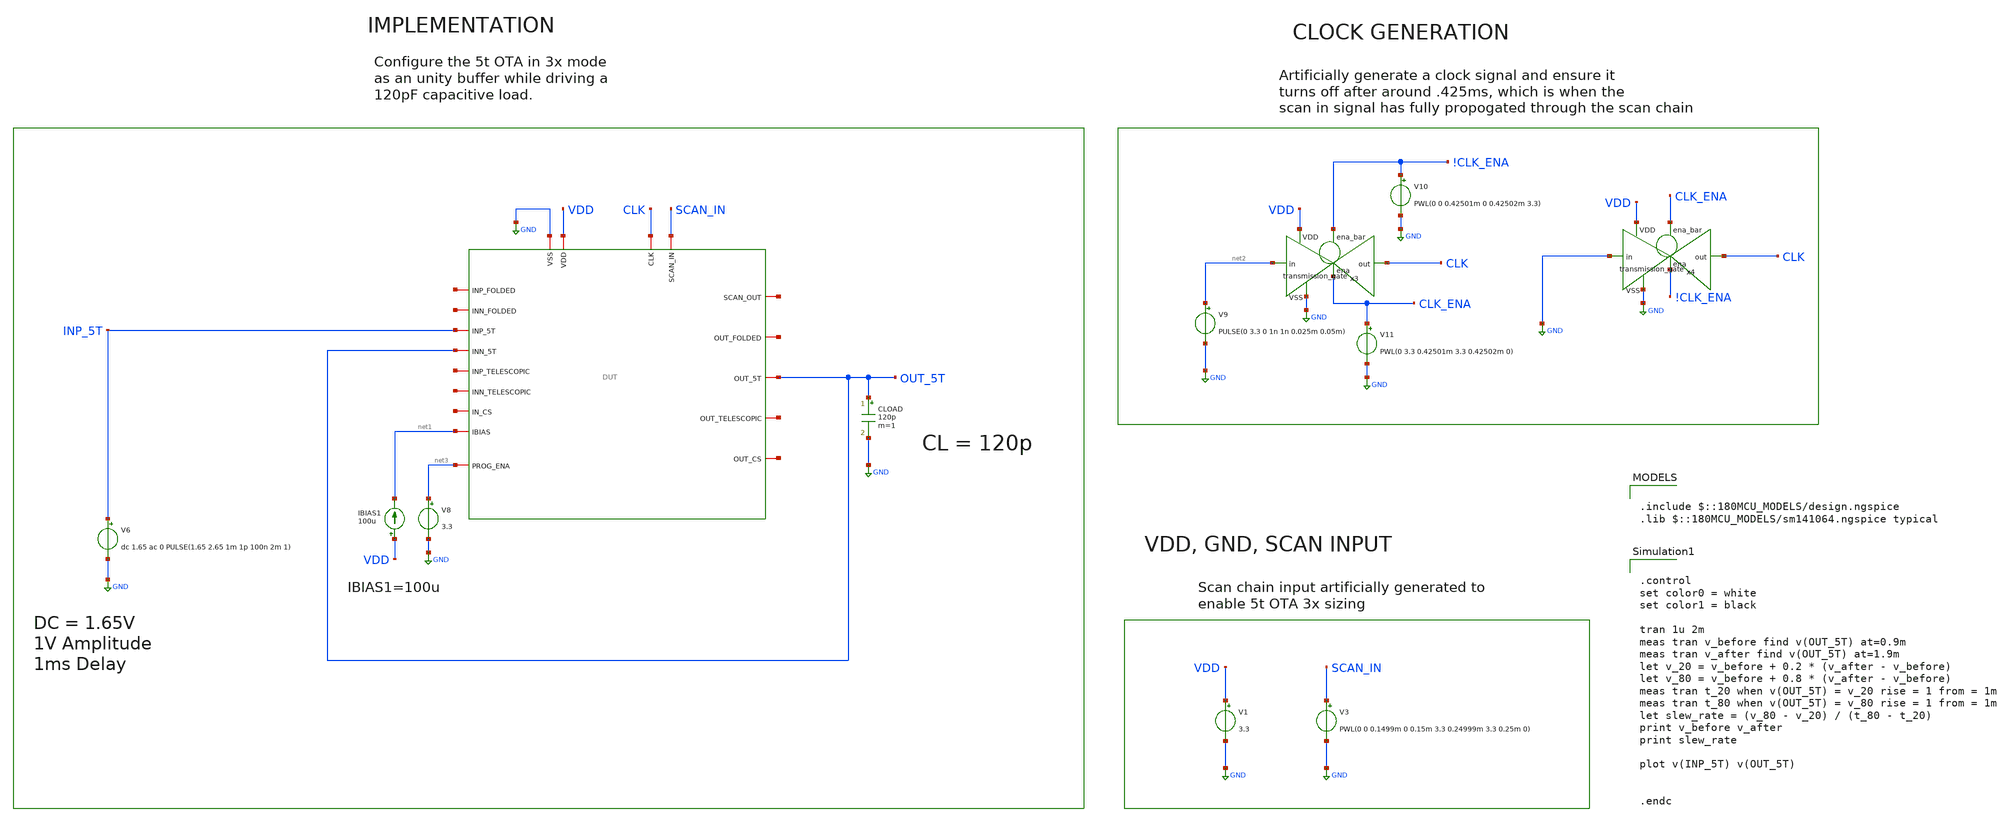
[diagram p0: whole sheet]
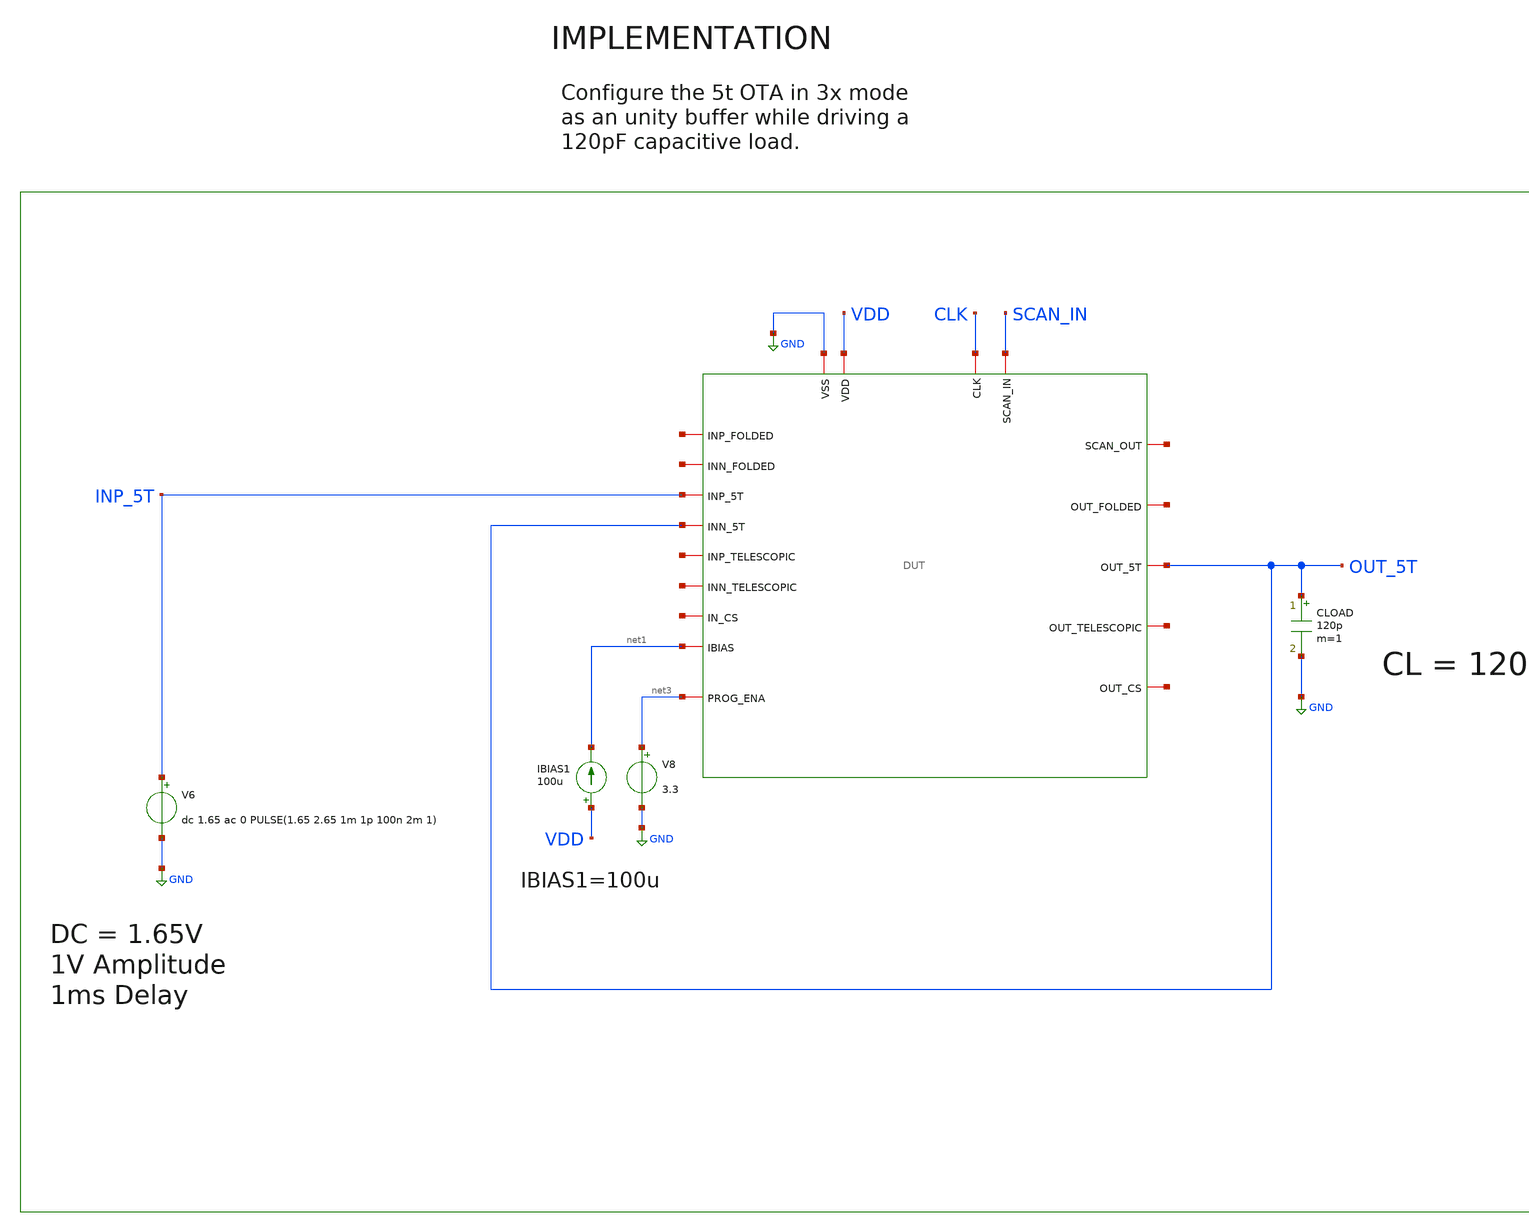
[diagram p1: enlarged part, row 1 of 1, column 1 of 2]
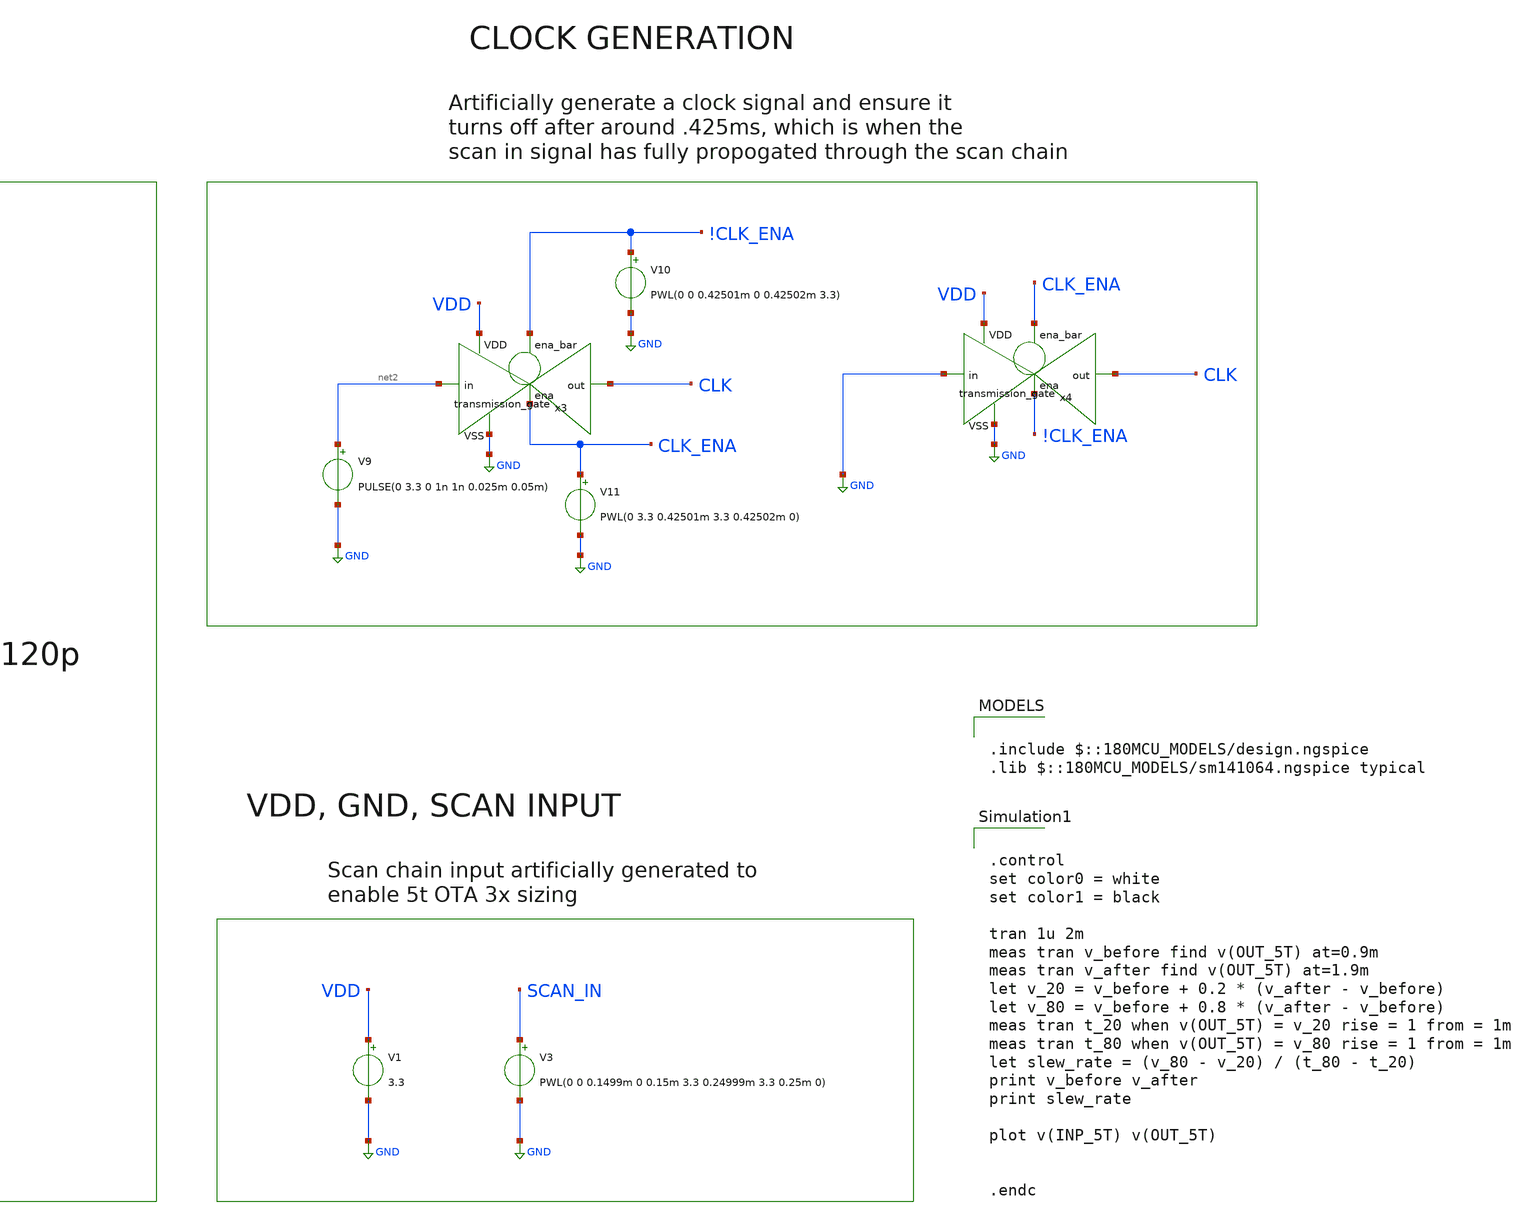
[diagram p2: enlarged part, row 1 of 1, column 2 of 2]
** sch_path: designs/libs/core_tb/sl/ota_5t/5t_tran_SR_3x.sch
**.subckt 5t_tran_SR_3x
V3 SCAN_IN GND PWL(0 0 0.1499m 0 0.15m 3.3 0.24999m 3.3 0.25m 0)
V1 VDD GND 3.3
IBIAS1 VDD net1 100u
CLOAD OUT_5T GND 120p m=1
V6 INP_5T GND dc 1.65 ac 0 PULSE(1.65 2.65 1m 1p 100n 2m 1)
x1 CLK net4 SCAN_IN GND VDD net5 net6 OUT_5T net1 net7 INP_5T OUT_5T net8 net9 net10 net11 net12
+ net3 DUT
V9 net2 GND PULSE(0 3.3 0 1n 1n 0.025m 0.05m)
x3 !CLK_ENA VDD CLK net2 GND CLK_ENA transmission_gate
V10 !CLK_ENA GND PWL(0 0 0.42501m 0 0.42502m 3.3)
V11 CLK_ENA GND PWL(0 3.3 0.42501m 3.3 0.42502m 0)
x4 CLK_ENA VDD CLK GND GND !CLK_ENA transmission_gate
V8 net3 GND 3.3
**** begin user architecture code

.include $::180MCU_MODELS/design.ngspice
.lib $::180MCU_MODELS/sm141064.ngspice typical



.control
set color0 = white
set color1 = black

tran 1u 2m
meas tran v_before find v(OUT_5T) at=0.9m
meas tran v_after find v(OUT_5T) at=1.9m
let v_20 = v_before + 0.2 * (v_after - v_before)
let v_80 = v_before + 0.8 * (v_after - v_before)
meas tran t_20 when v(OUT_5T) = v_20 rise = 1 from = 1m
meas tran t_80 when v(OUT_5T) = v_80 rise = 1 from = 1m
let slew_rate = (v_80 - v_20) / (t_80 - t_20)
print v_before v_after
print slew_rate

plot v(INP_5T) v(OUT_5T)


.endc


**** end user architecture code
**.ends
.GLOBAL GND
.end
